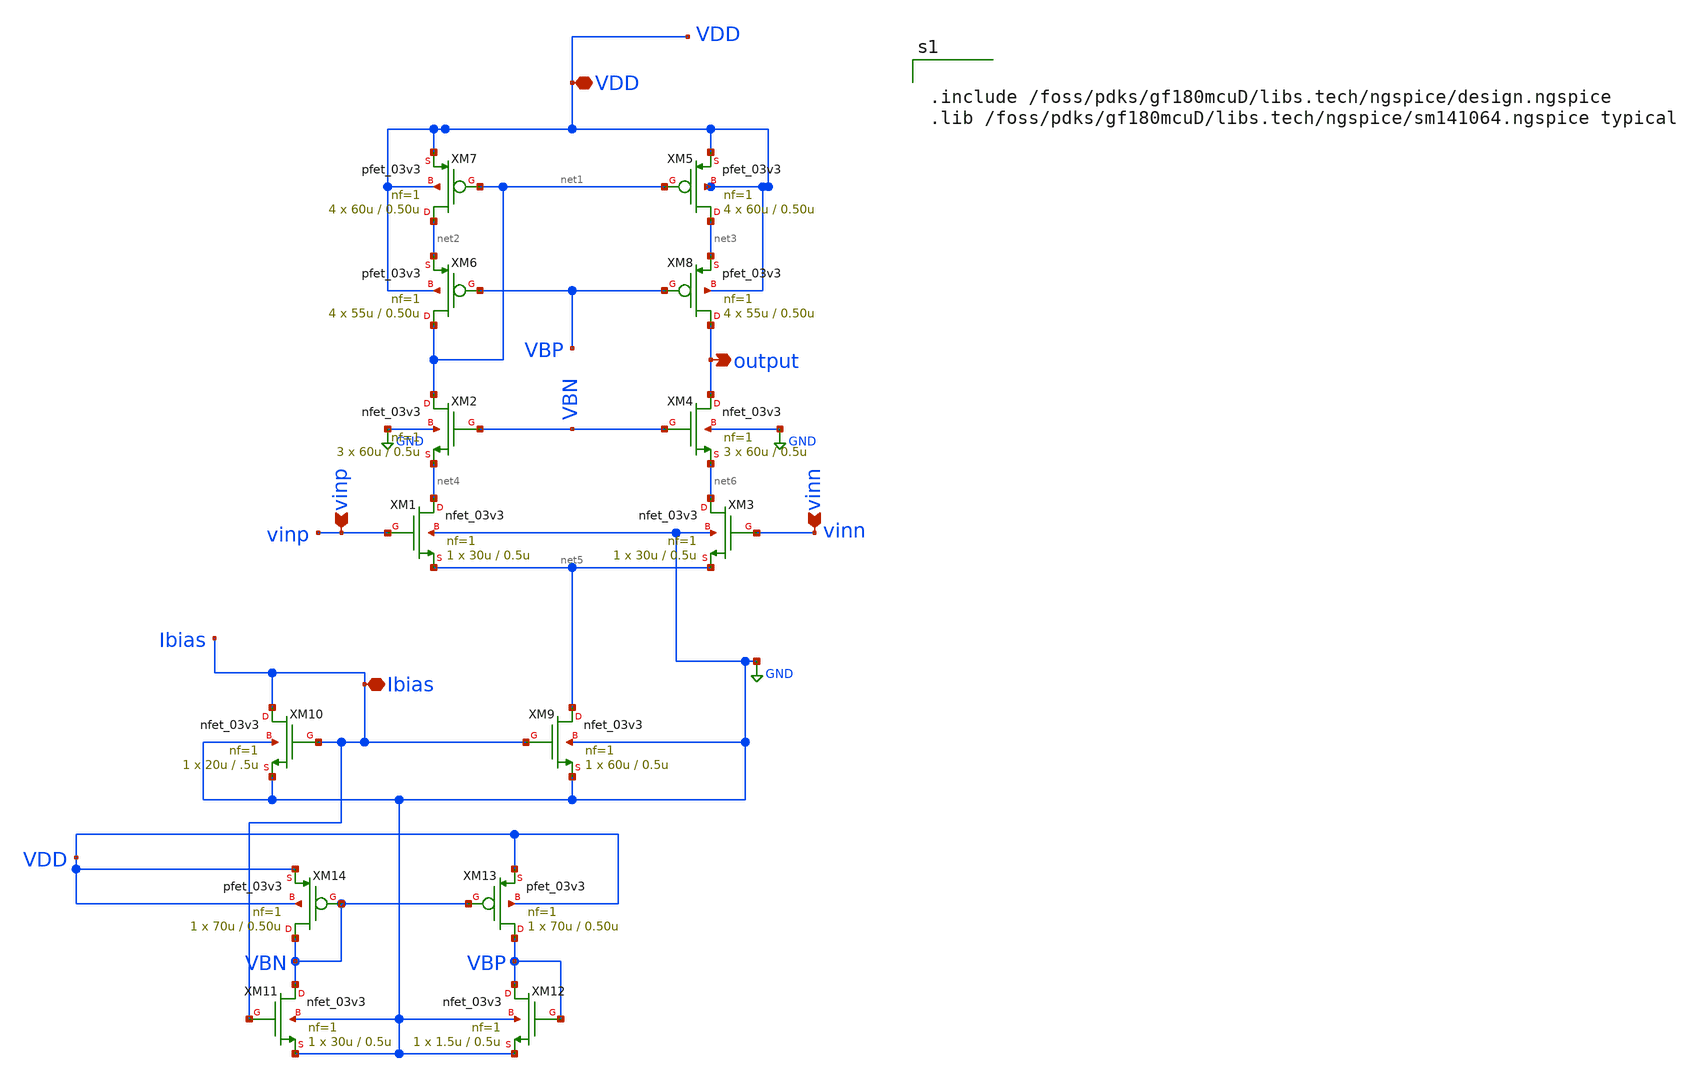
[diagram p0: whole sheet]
** sch_path: designs/libs/core_amps/ota_telescopic/telescopic_cascode.sch
**.subckt telescopic_cascode vinp vinn output Ibias VDD
*.ipin vinp
*.ipin vinn
*.opin output
*.iopin Ibias
*.iopin VDD
XM8 output VBP net3 VDD pfet_03v3 L=0.50u W=55u nf=1 ad='int((nf+1)/2) * W/nf * 0.18u' as='int((nf+2)/2) * W/nf * 0.18u'
+ pd='2*int((nf+1)/2) * (W/nf + 0.18u)' ps='2*int((nf+2)/2) * (W/nf + 0.18u)' nrd='0.18u / W' nrs='0.18u / W'
+ sa=0 sb=0 sd=0 m=4
XM4 output VBN net6 GND nfet_03v3 L=0.5u W=60u nf=1 ad='int((nf+1)/2) * W/nf * 0.18u' as='int((nf+2)/2) * W/nf * 0.18u'
+ pd='2*int((nf+1)/2) * (W/nf + 0.18u)' ps='2*int((nf+2)/2) * (W/nf + 0.18u)' nrd='0.18u / W' nrs='0.18u / W'
+ sa=0 sb=0 sd=0 m=3
XM1 net4 vinp net5 GND nfet_03v3 L=0.5u W=30u nf=1 ad='int((nf+1)/2) * W/nf * 0.18u' as='int((nf+2)/2) * W/nf * 0.18u'
+ pd='2*int((nf+1)/2) * (W/nf + 0.18u)' ps='2*int((nf+2)/2) * (W/nf + 0.18u)' nrd='0.18u / W' nrs='0.18u / W'
+ sa=0 sb=0 sd=0 m=1
XM2 net1 VBN net4 GND nfet_03v3 L=0.5u W=60u nf=1 ad='int((nf+1)/2) * W/nf * 0.18u' as='int((nf+2)/2) * W/nf * 0.18u'
+ pd='2*int((nf+1)/2) * (W/nf + 0.18u)' ps='2*int((nf+2)/2) * (W/nf + 0.18u)' nrd='0.18u / W' nrs='0.18u / W'
+ sa=0 sb=0 sd=0 m=3
XM3 net6 vinn net5 GND nfet_03v3 L=0.5u W=30u nf=1 ad='int((nf+1)/2) * W/nf * 0.18u' as='int((nf+2)/2) * W/nf * 0.18u'
+ pd='2*int((nf+1)/2) * (W/nf + 0.18u)' ps='2*int((nf+2)/2) * (W/nf + 0.18u)' nrd='0.18u / W' nrs='0.18u / W'
+ sa=0 sb=0 sd=0 m=1
XM5 net3 net1 VDD VDD pfet_03v3 L=0.50u W=60u nf=1 ad='int((nf+1)/2) * W/nf * 0.18u' as='int((nf+2)/2) * W/nf * 0.18u'
+ pd='2*int((nf+1)/2) * (W/nf + 0.18u)' ps='2*int((nf+2)/2) * (W/nf + 0.18u)' nrd='0.18u / W' nrs='0.18u / W'
+ sa=0 sb=0 sd=0 m=4
XM6 net1 VBP net2 VDD pfet_03v3 L=0.50u W=55u nf=1 ad='int((nf+1)/2) * W/nf * 0.18u' as='int((nf+2)/2) * W/nf * 0.18u'
+ pd='2*int((nf+1)/2) * (W/nf + 0.18u)' ps='2*int((nf+2)/2) * (W/nf + 0.18u)' nrd='0.18u / W' nrs='0.18u / W'
+ sa=0 sb=0 sd=0 m=4
XM7 net2 net1 VDD VDD pfet_03v3 L=0.50u W=60u nf=1 ad='int((nf+1)/2) * W/nf * 0.18u' as='int((nf+2)/2) * W/nf * 0.18u'
+ pd='2*int((nf+1)/2) * (W/nf + 0.18u)' ps='2*int((nf+2)/2) * (W/nf + 0.18u)' nrd='0.18u / W' nrs='0.18u / W'
+ sa=0 sb=0 sd=0 m=4
XM9 net5 Ibias GND GND nfet_03v3 L=0.5u W=60u nf=1 ad='int((nf+1)/2) * W/nf * 0.18u' as='int((nf+2)/2) * W/nf * 0.18u'
+ pd='2*int((nf+1)/2) * (W/nf + 0.18u)' ps='2*int((nf+2)/2) * (W/nf + 0.18u)' nrd='0.18u / W' nrs='0.18u / W'
+ sa=0 sb=0 sd=0 m=1
XM10 Ibias Ibias GND GND nfet_03v3 L=.5u W=20u nf=1 ad='int((nf+1)/2) * W/nf * 0.18u' as='int((nf+2)/2) * W/nf * 0.18u'
+ pd='2*int((nf+1)/2) * (W/nf + 0.18u)' ps='2*int((nf+2)/2) * (W/nf + 0.18u)' nrd='0.18u / W' nrs='0.18u / W'
+ sa=0 sb=0 sd=0 m=1
XM11 VBN Ibias GND GND nfet_03v3 L=0.5u W=30u nf=1 ad='int((nf+1)/2) * W/nf * 0.18u' as='int((nf+2)/2) * W/nf * 0.18u'
+ pd='2*int((nf+1)/2) * (W/nf + 0.18u)' ps='2*int((nf+2)/2) * (W/nf + 0.18u)' nrd='0.18u / W' nrs='0.18u / W'
+ sa=0 sb=0 sd=0 m=1
XM12 VBP VBP GND GND nfet_03v3 L=0.5u W=1.5u nf=1 ad='int((nf+1)/2) * W/nf * 0.18u' as='int((nf+2)/2) * W/nf * 0.18u'
+ pd='2*int((nf+1)/2) * (W/nf + 0.18u)' ps='2*int((nf+2)/2) * (W/nf + 0.18u)' nrd='0.18u / W' nrs='0.18u / W'
+ sa=0 sb=0 sd=0 m=1
XM13 VBP VBN VDD VDD pfet_03v3 L=0.50u W=70u nf=1 ad='int((nf+1)/2) * W/nf * 0.18u' as='int((nf+2)/2) * W/nf * 0.18u'
+ pd='2*int((nf+1)/2) * (W/nf + 0.18u)' ps='2*int((nf+2)/2) * (W/nf + 0.18u)' nrd='0.18u / W' nrs='0.18u / W'
+ sa=0 sb=0 sd=0 m=1
XM14 VBN VBN VDD VDD pfet_03v3 L=0.50u W=70u nf=1 ad='int((nf+1)/2) * W/nf * 0.18u' as='int((nf+2)/2) * W/nf * 0.18u'
+ pd='2*int((nf+1)/2) * (W/nf + 0.18u)' ps='2*int((nf+2)/2) * (W/nf + 0.18u)' nrd='0.18u / W' nrs='0.18u / W'
+ sa=0 sb=0 sd=0 m=1
**** begin user architecture code


.include /foss/pdks/gf180mcuD/libs.tech/ngspice/design.ngspice
.lib /foss/pdks/gf180mcuD/libs.tech/ngspice/sm141064.ngspice typical

**** end user architecture code
**.ends
.GLOBAL GND
.end
